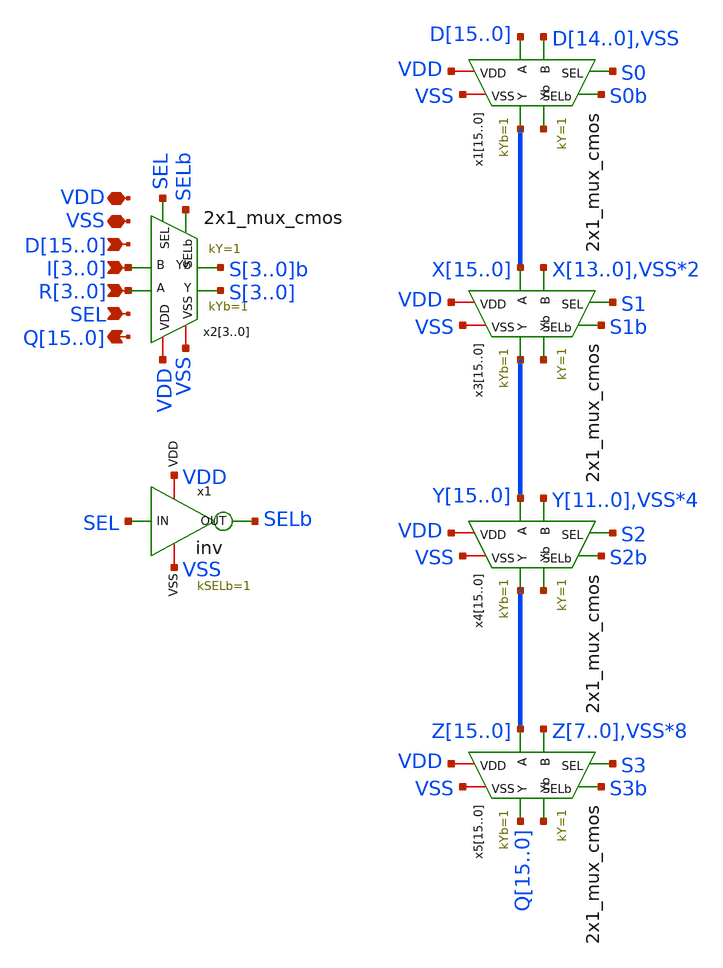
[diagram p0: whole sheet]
** sch_path: CAD5/shifter.sch
**.subckt shifter VDD VSS D15,D14,D13,D12,D11,D10,D9,D8,D7,D6,D5,D4,D3,D2,D1,D0
*+ Q15,Q14,Q13,Q12,Q11,Q10,Q9,Q8,Q7,Q6,Q5,Q4,Q3,Q2,Q1,Q0 R3,R2,R1,R0 I3,I2,I1,I0 SEL
*.iopin VDD
*.iopin VSS
*.ipin D15,D14,D13,D12,D11,D10,D9,D8,D7,D6,D5,D4,D3,D2,D1,D0
*.opin Q15,Q14,Q13,Q12,Q11,Q10,Q9,Q8,Q7,Q6,Q5,Q4,Q3,Q2,Q1,Q0
*.ipin R3,R2,R1,R0
*.ipin I3,I2,I1,I0
*.ipin SEL
x115 D15 S0 S0b X15 VDD VSS D14 net1[15] 2x1_mux_cmos kYb=1 kY=1
x114 D14 S0 S0b X14 VDD VSS D13 net1[14] 2x1_mux_cmos kYb=1 kY=1
x113 D13 S0 S0b X13 VDD VSS D12 net1[13] 2x1_mux_cmos kYb=1 kY=1
x112 D12 S0 S0b X12 VDD VSS D11 net1[12] 2x1_mux_cmos kYb=1 kY=1
x111 D11 S0 S0b X11 VDD VSS D10 net1[11] 2x1_mux_cmos kYb=1 kY=1
x110 D10 S0 S0b X10 VDD VSS D9 net1[10] 2x1_mux_cmos kYb=1 kY=1
x19 D9 S0 S0b X9 VDD VSS D8 net1[9] 2x1_mux_cmos kYb=1 kY=1
x18 D8 S0 S0b X8 VDD VSS D7 net1[8] 2x1_mux_cmos kYb=1 kY=1
x17 D7 S0 S0b X7 VDD VSS D6 net1[7] 2x1_mux_cmos kYb=1 kY=1
x16 D6 S0 S0b X6 VDD VSS D5 net1[6] 2x1_mux_cmos kYb=1 kY=1
x15 D5 S0 S0b X5 VDD VSS D4 net1[5] 2x1_mux_cmos kYb=1 kY=1
x14 D4 S0 S0b X4 VDD VSS D3 net1[4] 2x1_mux_cmos kYb=1 kY=1
x13 D3 S0 S0b X3 VDD VSS D2 net1[3] 2x1_mux_cmos kYb=1 kY=1
x12 D2 S0 S0b X2 VDD VSS D1 net1[2] 2x1_mux_cmos kYb=1 kY=1
x11 D1 S0 S0b X1 VDD VSS D0 net1[1] 2x1_mux_cmos kYb=1 kY=1
x10 D0 S0 S0b X0 VDD VSS VSS net1[0] 2x1_mux_cmos kYb=1 kY=1
x23 R3 SEL SELb S3 VDD VSS I3 S3b 2x1_mux_cmos kYb=1 kY=1
x22 R2 SEL SELb S2 VDD VSS I2 S2b 2x1_mux_cmos kYb=1 kY=1
x21 R1 SEL SELb S1 VDD VSS I1 S1b 2x1_mux_cmos kYb=1 kY=1
x20 R0 SEL SELb S0 VDD VSS I0 S0b 2x1_mux_cmos kYb=1 kY=1
x1 VDD SEL SELb VSS inv kSELb=1
x315 X15 S1 S1b Y15 VDD VSS X13 net2[15] 2x1_mux_cmos kYb=1 kY=1
x314 X14 S1 S1b Y14 VDD VSS X12 net2[14] 2x1_mux_cmos kYb=1 kY=1
x313 X13 S1 S1b Y13 VDD VSS X11 net2[13] 2x1_mux_cmos kYb=1 kY=1
x312 X12 S1 S1b Y12 VDD VSS X10 net2[12] 2x1_mux_cmos kYb=1 kY=1
x311 X11 S1 S1b Y11 VDD VSS X9 net2[11] 2x1_mux_cmos kYb=1 kY=1
x310 X10 S1 S1b Y10 VDD VSS X8 net2[10] 2x1_mux_cmos kYb=1 kY=1
x39 X9 S1 S1b Y9 VDD VSS X7 net2[9] 2x1_mux_cmos kYb=1 kY=1
x38 X8 S1 S1b Y8 VDD VSS X6 net2[8] 2x1_mux_cmos kYb=1 kY=1
x37 X7 S1 S1b Y7 VDD VSS X5 net2[7] 2x1_mux_cmos kYb=1 kY=1
x36 X6 S1 S1b Y6 VDD VSS X4 net2[6] 2x1_mux_cmos kYb=1 kY=1
x35 X5 S1 S1b Y5 VDD VSS X3 net2[5] 2x1_mux_cmos kYb=1 kY=1
x34 X4 S1 S1b Y4 VDD VSS X2 net2[4] 2x1_mux_cmos kYb=1 kY=1
x33 X3 S1 S1b Y3 VDD VSS X1 net2[3] 2x1_mux_cmos kYb=1 kY=1
x32 X2 S1 S1b Y2 VDD VSS X0 net2[2] 2x1_mux_cmos kYb=1 kY=1
x31 X1 S1 S1b Y1 VDD VSS VSS net2[1] 2x1_mux_cmos kYb=1 kY=1
x30 X0 S1 S1b Y0 VDD VSS VSS net2[0] 2x1_mux_cmos kYb=1 kY=1
x415 Y15 S2 S2b Z15 VDD VSS Y11 net3[15] 2x1_mux_cmos kYb=1 kY=1
x414 Y14 S2 S2b Z14 VDD VSS Y10 net3[14] 2x1_mux_cmos kYb=1 kY=1
x413 Y13 S2 S2b Z13 VDD VSS Y9 net3[13] 2x1_mux_cmos kYb=1 kY=1
x412 Y12 S2 S2b Z12 VDD VSS Y8 net3[12] 2x1_mux_cmos kYb=1 kY=1
x411 Y11 S2 S2b Z11 VDD VSS Y7 net3[11] 2x1_mux_cmos kYb=1 kY=1
x410 Y10 S2 S2b Z10 VDD VSS Y6 net3[10] 2x1_mux_cmos kYb=1 kY=1
x49 Y9 S2 S2b Z9 VDD VSS Y5 net3[9] 2x1_mux_cmos kYb=1 kY=1
x48 Y8 S2 S2b Z8 VDD VSS Y4 net3[8] 2x1_mux_cmos kYb=1 kY=1
x47 Y7 S2 S2b Z7 VDD VSS Y3 net3[7] 2x1_mux_cmos kYb=1 kY=1
x46 Y6 S2 S2b Z6 VDD VSS Y2 net3[6] 2x1_mux_cmos kYb=1 kY=1
x45 Y5 S2 S2b Z5 VDD VSS Y1 net3[5] 2x1_mux_cmos kYb=1 kY=1
x44 Y4 S2 S2b Z4 VDD VSS Y0 net3[4] 2x1_mux_cmos kYb=1 kY=1
x43 Y3 S2 S2b Z3 VDD VSS VSS net3[3] 2x1_mux_cmos kYb=1 kY=1
x42 Y2 S2 S2b Z2 VDD VSS VSS net3[2] 2x1_mux_cmos kYb=1 kY=1
x41 Y1 S2 S2b Z1 VDD VSS VSS net3[1] 2x1_mux_cmos kYb=1 kY=1
x40 Y0 S2 S2b Z0 VDD VSS VSS net3[0] 2x1_mux_cmos kYb=1 kY=1
x515 Z15 S3 S3b Q15 VDD VSS Z7 net4[15] 2x1_mux_cmos kYb=1 kY=1
x514 Z14 S3 S3b Q14 VDD VSS Z6 net4[14] 2x1_mux_cmos kYb=1 kY=1
x513 Z13 S3 S3b Q13 VDD VSS Z5 net4[13] 2x1_mux_cmos kYb=1 kY=1
x512 Z12 S3 S3b Q12 VDD VSS Z4 net4[12] 2x1_mux_cmos kYb=1 kY=1
x511 Z11 S3 S3b Q11 VDD VSS Z3 net4[11] 2x1_mux_cmos kYb=1 kY=1
x510 Z10 S3 S3b Q10 VDD VSS Z2 net4[10] 2x1_mux_cmos kYb=1 kY=1
x59 Z9 S3 S3b Q9 VDD VSS Z1 net4[9] 2x1_mux_cmos kYb=1 kY=1
x58 Z8 S3 S3b Q8 VDD VSS Z0 net4[8] 2x1_mux_cmos kYb=1 kY=1
x57 Z7 S3 S3b Q7 VDD VSS VSS net4[7] 2x1_mux_cmos kYb=1 kY=1
x56 Z6 S3 S3b Q6 VDD VSS VSS net4[6] 2x1_mux_cmos kYb=1 kY=1
x55 Z5 S3 S3b Q5 VDD VSS VSS net4[5] 2x1_mux_cmos kYb=1 kY=1
x54 Z4 S3 S3b Q4 VDD VSS VSS net4[4] 2x1_mux_cmos kYb=1 kY=1
x53 Z3 S3 S3b Q3 VDD VSS VSS net4[3] 2x1_mux_cmos kYb=1 kY=1
x52 Z2 S3 S3b Q2 VDD VSS VSS net4[2] 2x1_mux_cmos kYb=1 kY=1
x51 Z1 S3 S3b Q1 VDD VSS VSS net4[1] 2x1_mux_cmos kYb=1 kY=1
x50 Z0 S3 S3b Q0 VDD VSS VSS net4[0] 2x1_mux_cmos kYb=1 kY=1
**.ends

* expanding   symbol:  engn1600-team1/CAD5/2x1_mux_cmos.sym # of pins=8
** sym_path: CAD4/2x1_mux_cmos.sym
** sch_path: CAD4/2x1_mux_cmos.sch
.subckt 2x1_mux_cmos A SEL SELb Y VDD VSS B Yb  kYb=1 kY=1
*.ipin A
*.ipin B
*.ipin SEL
*.opin Y
*.iopin VDD
*.iopin VSS
*.ipin SELb
*.opin Yb
XM1 VSS B net1 VSS nfet_03v3 L=0.28u W='kI*0.36u' nf=1 ad='int((nf+1)/2) * W/nf * 0.18u' as='int((nf+2)/2) * W/nf * 0.18u'
+ pd='2*int((nf+1)/2) * (W/nf + 0.18u)' ps='2*int((nf+2)/2) * (W/nf + 0.18u)' nrd='0.18u / W' nrs='0.18u / W'
+ sa=0 sb=0 sd=0 m=1
XM2 net1 SEL Yb VSS nfet_03v3 L=0.28u W='kYb*0.36u' nf=1 ad='int((nf+1)/2) * W/nf * 0.18u' as='int((nf+2)/2) * W/nf * 0.18u'
+ pd='2*int((nf+1)/2) * (W/nf + 0.18u)' ps='2*int((nf+2)/2) * (W/nf + 0.18u)' nrd='0.18u / W' nrs='0.18u / W'
+ sa=0 sb=0 sd=0 m=1
XM3 Yb SELb net2 VSS nfet_03v3 L=0.28u W='kYb*0.36u' nf=1 ad='int((nf+1)/2) * W/nf * 0.18u' as='int((nf+2)/2) * W/nf * 0.18u'
+ pd='2*int((nf+1)/2) * (W/nf + 0.18u)' ps='2*int((nf+2)/2) * (W/nf + 0.18u)' nrd='0.18u / W' nrs='0.18u / W'
+ sa=0 sb=0 sd=0 m=1
XM4 net2 A VSS VSS nfet_03v3 L=0.28u W='kI*0.36u' nf=1 ad='int((nf+1)/2) * W/nf * 0.18u' as='int((nf+2)/2) * W/nf * 0.18u'
+ pd='2*int((nf+1)/2) * (W/nf + 0.18u)' ps='2*int((nf+2)/2) * (W/nf + 0.18u)' nrd='0.18u / W' nrs='0.18u / W'
+ sa=0 sb=0 sd=0 m=1
XM5 net3 SELb Yb VDD pfet_03v3 L=0.28u W='kYb*0.72u' nf=1 ad='int((nf+1)/2) * W/nf * 0.18u' as='int((nf+2)/2) * W/nf * 0.18u'
+ pd='2*int((nf+1)/2) * (W/nf + 0.18u)' ps='2*int((nf+2)/2) * (W/nf + 0.18u)' nrd='0.18u / W' nrs='0.18u / W'
+ sa=0 sb=0 sd=0 m=1
XM6 VDD B net3 VDD pfet_03v3 L=0.28u W='kI*0.72u' nf=1 ad='int((nf+1)/2) * W/nf * 0.18u' as='int((nf+2)/2) * W/nf * 0.18u'
+ pd='2*int((nf+1)/2) * (W/nf + 0.18u)' ps='2*int((nf+2)/2) * (W/nf + 0.18u)' nrd='0.18u / W' nrs='0.18u / W'
+ sa=0 sb=0 sd=0 m=1
XM7 net4 A VDD VDD pfet_03v3 L=0.28u W='kI*0.72u' nf=1 ad='int((nf+1)/2) * W/nf * 0.18u' as='int((nf+2)/2) * W/nf * 0.18u'
+ pd='2*int((nf+1)/2) * (W/nf + 0.18u)' ps='2*int((nf+2)/2) * (W/nf + 0.18u)' nrd='0.18u / W' nrs='0.18u / W'
+ sa=0 sb=0 sd=0 m=1
XM8 Yb SEL net4 VDD pfet_03v3 L=0.28u W='kYb*0.72u' nf=1 ad='int((nf+1)/2) * W/nf * 0.18u' as='int((nf+2)/2) * W/nf * 0.18u'
+ pd='2*int((nf+1)/2) * (W/nf + 0.18u)' ps='2*int((nf+2)/2) * (W/nf + 0.18u)' nrd='0.18u / W' nrs='0.18u / W'
+ sa=0 sb=0 sd=0 m=1
XM9 VSS Yb Y VSS nfet_03v3 L=0.28u W='kY*0.36u' nf=1 ad='int((nf+1)/2) * W/nf * 0.18u' as='int((nf+2)/2) * W/nf * 0.18u'
+ pd='2*int((nf+1)/2) * (W/nf + 0.18u)' ps='2*int((nf+2)/2) * (W/nf + 0.18u)' nrd='0.18u / W' nrs='0.18u / W'
+ sa=0 sb=0 sd=0 m=1
XM10 VDD Yb Y VDD pfet_03v3 L=0.28u W='kY*0.72u' nf=1 ad='int((nf+1)/2) * W/nf * 0.18u' as='int((nf+2)/2) * W/nf * 0.18u'
+ pd='2*int((nf+1)/2) * (W/nf + 0.18u)' ps='2*int((nf+2)/2) * (W/nf + 0.18u)' nrd='0.18u / W' nrs='0.18u / W'
+ sa=0 sb=0 sd=0 m=1
**** begin user architecture code


.param kI=2.5
.param kYb=1.875
.param kY=2.1527777777777778


**** end user architecture code
.ends


* expanding   symbol:  engn1600-team1/CAD5/inv.sym # of pins=4
** sym_path: CAD5/inv.sym
** sch_path: CAD5/inv.sch
.subckt inv VDD IN OUT VSS  kSELb=1
*.ipin IN
*.opin OUT
*.iopin VDD
*.iopin VSS
XM1 OUT IN VDD VDD pfet_03v3 L=0.28u W='kSELb*0.72u' nf=1 ad='int((nf+1)/2) * W/nf * 0.18u' as='int((nf+2)/2) * W/nf * 0.18u'
+ pd='2*int((nf+1)/2) * (W/nf + 0.18u)' ps='2*int((nf+2)/2) * (W/nf + 0.18u)' nrd='0.18u / W' nrs='0.18u / W'
+ sa=0 sb=0 sd=0 m=1
XM2 OUT IN VSS VSS nfet_03v3 L=0.28u W='kSELb*0.36u' nf=1 ad='int((nf+1)/2) * W/nf * 0.18u' as='int((nf+2)/2) * W/nf * 0.18u'
+ pd='2*int((nf+1)/2) * (W/nf + 0.18u)' ps='2*int((nf+2)/2) * (W/nf + 0.18u)' nrd='0.18u / W' nrs='0.18u / W'
+ sa=0 sb=0 sd=0 m=1
**** begin user architecture code


.param kSELb=1


**** end user architecture code
.ends

.end
